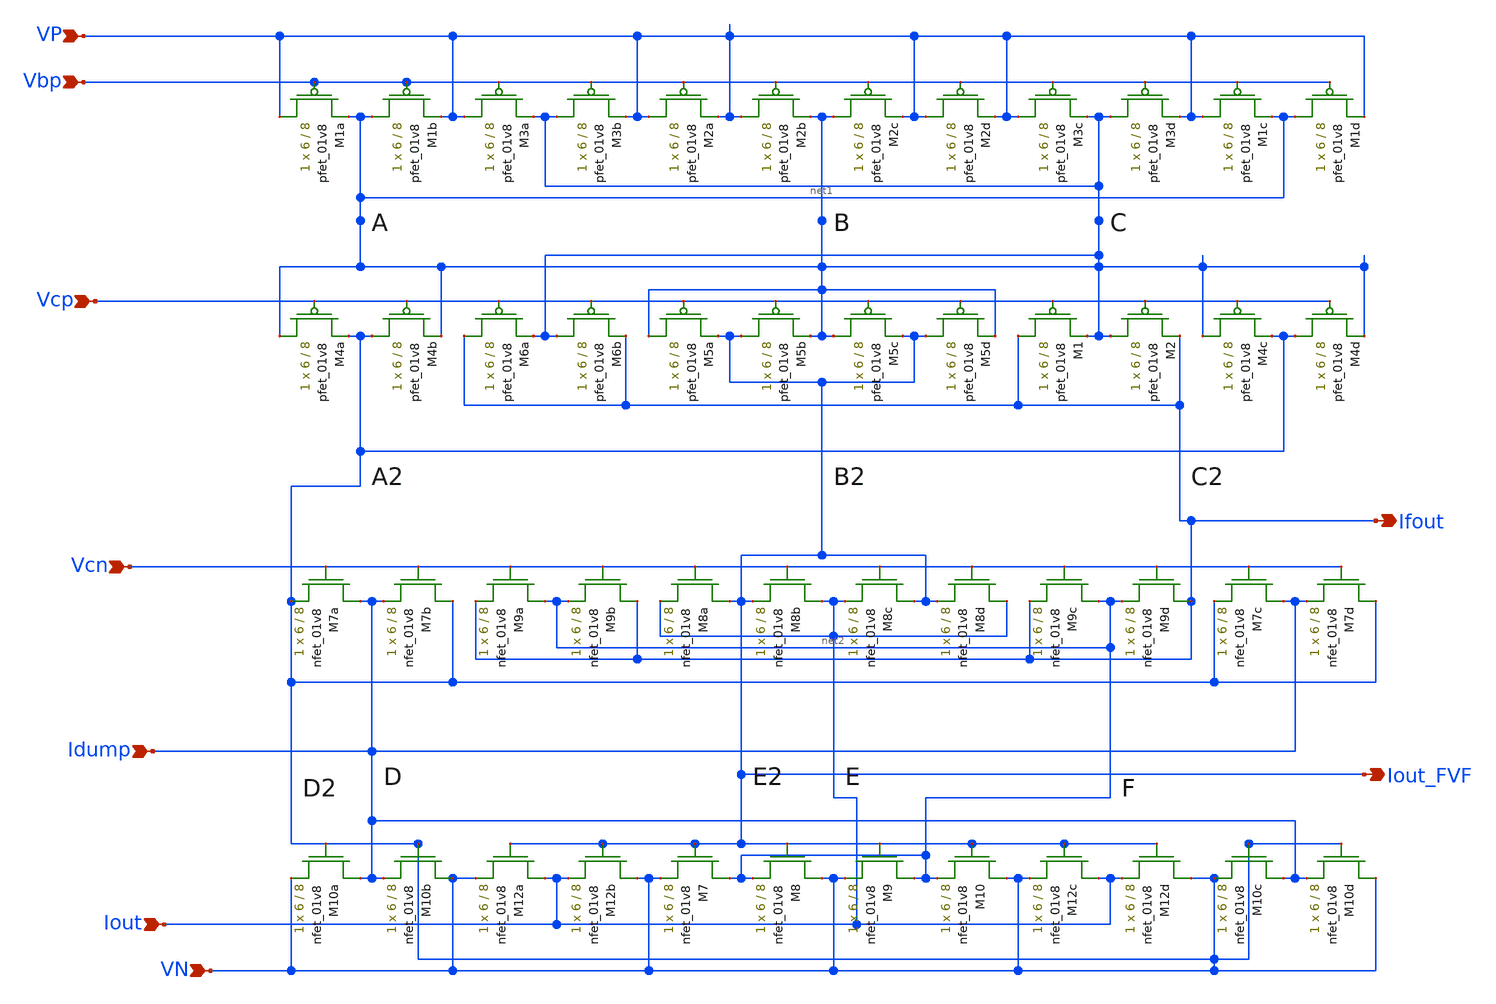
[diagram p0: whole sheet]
** sch_path: xschem/lds/lds-fvf-j.sch
**.subckt lds-fvf-j Vbp VP Vcp Vcn VN Idump Iout Ifout Iout_FVF
*.ipin Vbp
*.ipin VP
*.ipin Vcp
*.ipin Vcn
*.ipin VN
*.ipin Idump
*.ipin Iout
*.opin Ifout
*.opin Iout_FVF
XM1a VP Vbp net1 VDD sky130_fd_pr__pfet_01v8 L=8 W=6 nf=1 ad='int((nf+1)/2) * W/nf * 0.29' as='int((nf+2)/2) * W/nf * 0.29'
+ pd='2*int((nf+1)/2) * (W/nf + 0.29)' ps='2*int((nf+2)/2) * (W/nf + 0.29)' nrd='0.29 / W' nrs='0.29 / W'
+ sa=0 sb=0 sd=0 mult=1 m=1
XM1b net1 Vbp VP VDD sky130_fd_pr__pfet_01v8 L=8 W=6 nf=1 ad='int((nf+1)/2) * W/nf * 0.29' as='int((nf+2)/2) * W/nf * 0.29'
+ pd='2*int((nf+1)/2) * (W/nf + 0.29)' ps='2*int((nf+2)/2) * (W/nf + 0.29)' nrd='0.29 / W' nrs='0.29 / W'
+ sa=0 sb=0 sd=0 mult=1 m=1
XM3a VP Vbp net1 VDD sky130_fd_pr__pfet_01v8 L=8 W=6 nf=1 ad='int((nf+1)/2) * W/nf * 0.29' as='int((nf+2)/2) * W/nf * 0.29'
+ pd='2*int((nf+1)/2) * (W/nf + 0.29)' ps='2*int((nf+2)/2) * (W/nf + 0.29)' nrd='0.29 / W' nrs='0.29 / W'
+ sa=0 sb=0 sd=0 mult=1 m=1
XM3b net1 Vbp VP VDD sky130_fd_pr__pfet_01v8 L=8 W=6 nf=1 ad='int((nf+1)/2) * W/nf * 0.29' as='int((nf+2)/2) * W/nf * 0.29'
+ pd='2*int((nf+1)/2) * (W/nf + 0.29)' ps='2*int((nf+2)/2) * (W/nf + 0.29)' nrd='0.29 / W' nrs='0.29 / W'
+ sa=0 sb=0 sd=0 mult=1 m=1
XM2a VP Vbp VP VDD sky130_fd_pr__pfet_01v8 L=8 W=6 nf=1 ad='int((nf+1)/2) * W/nf * 0.29' as='int((nf+2)/2) * W/nf * 0.29'
+ pd='2*int((nf+1)/2) * (W/nf + 0.29)' ps='2*int((nf+2)/2) * (W/nf + 0.29)' nrd='0.29 / W' nrs='0.29 / W'
+ sa=0 sb=0 sd=0 mult=1 m=1
XM2b VP Vbp net1 VDD sky130_fd_pr__pfet_01v8 L=8 W=6 nf=1 ad='int((nf+1)/2) * W/nf * 0.29' as='int((nf+2)/2) * W/nf * 0.29'
+ pd='2*int((nf+1)/2) * (W/nf + 0.29)' ps='2*int((nf+2)/2) * (W/nf + 0.29)' nrd='0.29 / W' nrs='0.29 / W'
+ sa=0 sb=0 sd=0 mult=1 m=1
XM2c net1 Vbp VP VDD sky130_fd_pr__pfet_01v8 L=8 W=6 nf=1 ad='int((nf+1)/2) * W/nf * 0.29' as='int((nf+2)/2) * W/nf * 0.29'
+ pd='2*int((nf+1)/2) * (W/nf + 0.29)' ps='2*int((nf+2)/2) * (W/nf + 0.29)' nrd='0.29 / W' nrs='0.29 / W'
+ sa=0 sb=0 sd=0 mult=1 m=1
XM2d VP Vbp VP VDD sky130_fd_pr__pfet_01v8 L=8 W=6 nf=1 ad='int((nf+1)/2) * W/nf * 0.29' as='int((nf+2)/2) * W/nf * 0.29'
+ pd='2*int((nf+1)/2) * (W/nf + 0.29)' ps='2*int((nf+2)/2) * (W/nf + 0.29)' nrd='0.29 / W' nrs='0.29 / W'
+ sa=0 sb=0 sd=0 mult=1 m=1
XM3c VP Vbp net1 VDD sky130_fd_pr__pfet_01v8 L=8 W=6 nf=1 ad='int((nf+1)/2) * W/nf * 0.29' as='int((nf+2)/2) * W/nf * 0.29'
+ pd='2*int((nf+1)/2) * (W/nf + 0.29)' ps='2*int((nf+2)/2) * (W/nf + 0.29)' nrd='0.29 / W' nrs='0.29 / W'
+ sa=0 sb=0 sd=0 mult=1 m=1
XM3d net1 Vbp VP VDD sky130_fd_pr__pfet_01v8 L=8 W=6 nf=1 ad='int((nf+1)/2) * W/nf * 0.29' as='int((nf+2)/2) * W/nf * 0.29'
+ pd='2*int((nf+1)/2) * (W/nf + 0.29)' ps='2*int((nf+2)/2) * (W/nf + 0.29)' nrd='0.29 / W' nrs='0.29 / W'
+ sa=0 sb=0 sd=0 mult=1 m=1
XM1c VP Vbp net1 VDD sky130_fd_pr__pfet_01v8 L=8 W=6 nf=1 ad='int((nf+1)/2) * W/nf * 0.29' as='int((nf+2)/2) * W/nf * 0.29'
+ pd='2*int((nf+1)/2) * (W/nf + 0.29)' ps='2*int((nf+2)/2) * (W/nf + 0.29)' nrd='0.29 / W' nrs='0.29 / W'
+ sa=0 sb=0 sd=0 mult=1 m=1
XM1d net1 Vbp VP VDD sky130_fd_pr__pfet_01v8 L=8 W=6 nf=1 ad='int((nf+1)/2) * W/nf * 0.29' as='int((nf+2)/2) * W/nf * 0.29'
+ pd='2*int((nf+1)/2) * (W/nf + 0.29)' ps='2*int((nf+2)/2) * (W/nf + 0.29)' nrd='0.29 / W' nrs='0.29 / W'
+ sa=0 sb=0 sd=0 mult=1 m=1
XM4a net1 Vcp VN VDD sky130_fd_pr__pfet_01v8 L=8 W=6 nf=1 ad='int((nf+1)/2) * W/nf * 0.29' as='int((nf+2)/2) * W/nf * 0.29'
+ pd='2*int((nf+1)/2) * (W/nf + 0.29)' ps='2*int((nf+2)/2) * (W/nf + 0.29)' nrd='0.29 / W' nrs='0.29 / W'
+ sa=0 sb=0 sd=0 mult=1 m=1
XM4b VN Vcp net1 VDD sky130_fd_pr__pfet_01v8 L=8 W=6 nf=1 ad='int((nf+1)/2) * W/nf * 0.29' as='int((nf+2)/2) * W/nf * 0.29'
+ pd='2*int((nf+1)/2) * (W/nf + 0.29)' ps='2*int((nf+2)/2) * (W/nf + 0.29)' nrd='0.29 / W' nrs='0.29 / W'
+ sa=0 sb=0 sd=0 mult=1 m=1
XM6a Ifout Vcp net1 VDD sky130_fd_pr__pfet_01v8 L=8 W=6 nf=1 ad='int((nf+1)/2) * W/nf * 0.29' as='int((nf+2)/2) * W/nf * 0.29'
+ pd='2*int((nf+1)/2) * (W/nf + 0.29)' ps='2*int((nf+2)/2) * (W/nf + 0.29)' nrd='0.29 / W' nrs='0.29 / W'
+ sa=0 sb=0 sd=0 mult=1 m=1
XM6b net1 Vcp Ifout VDD sky130_fd_pr__pfet_01v8 L=8 W=6 nf=1 ad='int((nf+1)/2) * W/nf * 0.29' as='int((nf+2)/2) * W/nf * 0.29'
+ pd='2*int((nf+1)/2) * (W/nf + 0.29)' ps='2*int((nf+2)/2) * (W/nf + 0.29)' nrd='0.29 / W' nrs='0.29 / W'
+ sa=0 sb=0 sd=0 mult=1 m=1
XM5a net1 Vcp Iout_FVF VDD sky130_fd_pr__pfet_01v8 L=8 W=6 nf=1 ad='int((nf+1)/2) * W/nf * 0.29' as='int((nf+2)/2) * W/nf * 0.29'
+ pd='2*int((nf+1)/2) * (W/nf + 0.29)' ps='2*int((nf+2)/2) * (W/nf + 0.29)' nrd='0.29 / W' nrs='0.29 / W'
+ sa=0 sb=0 sd=0 mult=1 m=1
XM5b Iout_FVF Vcp net1 VDD sky130_fd_pr__pfet_01v8 L=8 W=6 nf=1 ad='int((nf+1)/2) * W/nf * 0.29' as='int((nf+2)/2) * W/nf * 0.29'
+ pd='2*int((nf+1)/2) * (W/nf + 0.29)' ps='2*int((nf+2)/2) * (W/nf + 0.29)' nrd='0.29 / W' nrs='0.29 / W'
+ sa=0 sb=0 sd=0 mult=1 m=1
XM5c net1 Vcp Iout_FVF VDD sky130_fd_pr__pfet_01v8 L=8 W=6 nf=1 ad='int((nf+1)/2) * W/nf * 0.29' as='int((nf+2)/2) * W/nf * 0.29'
+ pd='2*int((nf+1)/2) * (W/nf + 0.29)' ps='2*int((nf+2)/2) * (W/nf + 0.29)' nrd='0.29 / W' nrs='0.29 / W'
+ sa=0 sb=0 sd=0 mult=1 m=1
XM5d Iout_FVF Vcp net1 VDD sky130_fd_pr__pfet_01v8 L=8 W=6 nf=1 ad='int((nf+1)/2) * W/nf * 0.29' as='int((nf+2)/2) * W/nf * 0.29'
+ pd='2*int((nf+1)/2) * (W/nf + 0.29)' ps='2*int((nf+2)/2) * (W/nf + 0.29)' nrd='0.29 / W' nrs='0.29 / W'
+ sa=0 sb=0 sd=0 mult=1 m=1
XM1 Ifout Vcp net1 VDD sky130_fd_pr__pfet_01v8 L=8 W=6 nf=1 ad='int((nf+1)/2) * W/nf * 0.29' as='int((nf+2)/2) * W/nf * 0.29'
+ pd='2*int((nf+1)/2) * (W/nf + 0.29)' ps='2*int((nf+2)/2) * (W/nf + 0.29)' nrd='0.29 / W' nrs='0.29 / W'
+ sa=0 sb=0 sd=0 mult=1 m=1
XM2 net1 Vcp Ifout VDD sky130_fd_pr__pfet_01v8 L=8 W=6 nf=1 ad='int((nf+1)/2) * W/nf * 0.29' as='int((nf+2)/2) * W/nf * 0.29'
+ pd='2*int((nf+1)/2) * (W/nf + 0.29)' ps='2*int((nf+2)/2) * (W/nf + 0.29)' nrd='0.29 / W' nrs='0.29 / W'
+ sa=0 sb=0 sd=0 mult=1 m=1
XM4c net1 Vcp VN VDD sky130_fd_pr__pfet_01v8 L=8 W=6 nf=1 ad='int((nf+1)/2) * W/nf * 0.29' as='int((nf+2)/2) * W/nf * 0.29'
+ pd='2*int((nf+1)/2) * (W/nf + 0.29)' ps='2*int((nf+2)/2) * (W/nf + 0.29)' nrd='0.29 / W' nrs='0.29 / W'
+ sa=0 sb=0 sd=0 mult=1 m=1
XM4d VN Vcp net1 VDD sky130_fd_pr__pfet_01v8 L=8 W=6 nf=1 ad='int((nf+1)/2) * W/nf * 0.29' as='int((nf+2)/2) * W/nf * 0.29'
+ pd='2*int((nf+1)/2) * (W/nf + 0.29)' ps='2*int((nf+2)/2) * (W/nf + 0.29)' nrd='0.29 / W' nrs='0.29 / W'
+ sa=0 sb=0 sd=0 mult=1 m=1
XM7a Idump Vcn VN GND sky130_fd_pr__nfet_01v8 L=8 W=6 nf=1 ad='int((nf+1)/2) * W/nf * 0.29' as='int((nf+2)/2) * W/nf * 0.29'
+ pd='2*int((nf+1)/2) * (W/nf + 0.29)' ps='2*int((nf+2)/2) * (W/nf + 0.29)' nrd='0.29 / W' nrs='0.29 / W'
+ sa=0 sb=0 sd=0 mult=1 m=1
XM7b VN Vcn Idump GND sky130_fd_pr__nfet_01v8 L=8 W=6 nf=1 ad='int((nf+1)/2) * W/nf * 0.29' as='int((nf+2)/2) * W/nf * 0.29'
+ pd='2*int((nf+1)/2) * (W/nf + 0.29)' ps='2*int((nf+2)/2) * (W/nf + 0.29)' nrd='0.29 / W' nrs='0.29 / W'
+ sa=0 sb=0 sd=0 mult=1 m=1
XM9a net2 Vcn Ifout GND sky130_fd_pr__nfet_01v8 L=8 W=6 nf=1 ad='int((nf+1)/2) * W/nf * 0.29' as='int((nf+2)/2) * W/nf * 0.29'
+ pd='2*int((nf+1)/2) * (W/nf + 0.29)' ps='2*int((nf+2)/2) * (W/nf + 0.29)' nrd='0.29 / W' nrs='0.29 / W'
+ sa=0 sb=0 sd=0 mult=1 m=1
XM9b Ifout Vcn net2 GND sky130_fd_pr__nfet_01v8 L=8 W=6 nf=1 ad='int((nf+1)/2) * W/nf * 0.29' as='int((nf+2)/2) * W/nf * 0.29'
+ pd='2*int((nf+1)/2) * (W/nf + 0.29)' ps='2*int((nf+2)/2) * (W/nf + 0.29)' nrd='0.29 / W' nrs='0.29 / W'
+ sa=0 sb=0 sd=0 mult=1 m=1
XM8a Iout_FVF Vcn Iout GND sky130_fd_pr__nfet_01v8 L=8 W=6 nf=1 ad='int((nf+1)/2) * W/nf * 0.29' as='int((nf+2)/2) * W/nf * 0.29'
+ pd='2*int((nf+1)/2) * (W/nf + 0.29)' ps='2*int((nf+2)/2) * (W/nf + 0.29)' nrd='0.29 / W' nrs='0.29 / W'
+ sa=0 sb=0 sd=0 mult=1 m=1
XM8b Iout Vcn Iout_FVF GND sky130_fd_pr__nfet_01v8 L=8 W=6 nf=1 ad='int((nf+1)/2) * W/nf * 0.29' as='int((nf+2)/2) * W/nf * 0.29'
+ pd='2*int((nf+1)/2) * (W/nf + 0.29)' ps='2*int((nf+2)/2) * (W/nf + 0.29)' nrd='0.29 / W' nrs='0.29 / W'
+ sa=0 sb=0 sd=0 mult=1 m=1
XM8c Iout_FVF Vcn Iout GND sky130_fd_pr__nfet_01v8 L=8 W=6 nf=1 ad='int((nf+1)/2) * W/nf * 0.29' as='int((nf+2)/2) * W/nf * 0.29'
+ pd='2*int((nf+1)/2) * (W/nf + 0.29)' ps='2*int((nf+2)/2) * (W/nf + 0.29)' nrd='0.29 / W' nrs='0.29 / W'
+ sa=0 sb=0 sd=0 mult=1 m=1
XM8d Iout Vcn Iout_FVF GND sky130_fd_pr__nfet_01v8 L=8 W=6 nf=1 ad='int((nf+1)/2) * W/nf * 0.29' as='int((nf+2)/2) * W/nf * 0.29'
+ pd='2*int((nf+1)/2) * (W/nf + 0.29)' ps='2*int((nf+2)/2) * (W/nf + 0.29)' nrd='0.29 / W' nrs='0.29 / W'
+ sa=0 sb=0 sd=0 mult=1 m=1
XM9c net2 Vcn Ifout GND sky130_fd_pr__nfet_01v8 L=8 W=6 nf=1 ad='int((nf+1)/2) * W/nf * 0.29' as='int((nf+2)/2) * W/nf * 0.29'
+ pd='2*int((nf+1)/2) * (W/nf + 0.29)' ps='2*int((nf+2)/2) * (W/nf + 0.29)' nrd='0.29 / W' nrs='0.29 / W'
+ sa=0 sb=0 sd=0 mult=1 m=1
XM9d Ifout Vcn net2 GND sky130_fd_pr__nfet_01v8 L=8 W=6 nf=1 ad='int((nf+1)/2) * W/nf * 0.29' as='int((nf+2)/2) * W/nf * 0.29'
+ pd='2*int((nf+1)/2) * (W/nf + 0.29)' ps='2*int((nf+2)/2) * (W/nf + 0.29)' nrd='0.29 / W' nrs='0.29 / W'
+ sa=0 sb=0 sd=0 mult=1 m=1
XM7c Idump Vcn VN GND sky130_fd_pr__nfet_01v8 L=8 W=6 nf=1 ad='int((nf+1)/2) * W/nf * 0.29' as='int((nf+2)/2) * W/nf * 0.29'
+ pd='2*int((nf+1)/2) * (W/nf + 0.29)' ps='2*int((nf+2)/2) * (W/nf + 0.29)' nrd='0.29 / W' nrs='0.29 / W'
+ sa=0 sb=0 sd=0 mult=1 m=1
XM7d VN Vcn Idump GND sky130_fd_pr__nfet_01v8 L=8 W=6 nf=1 ad='int((nf+1)/2) * W/nf * 0.29' as='int((nf+2)/2) * W/nf * 0.29'
+ pd='2*int((nf+1)/2) * (W/nf + 0.29)' ps='2*int((nf+2)/2) * (W/nf + 0.29)' nrd='0.29 / W' nrs='0.29 / W'
+ sa=0 sb=0 sd=0 mult=1 m=1
XM10a Idump VN VN GND sky130_fd_pr__nfet_01v8 L=8 W=6 nf=1 ad='int((nf+1)/2) * W/nf * 0.29' as='int((nf+2)/2) * W/nf * 0.29'
+ pd='2*int((nf+1)/2) * (W/nf + 0.29)' ps='2*int((nf+2)/2) * (W/nf + 0.29)' nrd='0.29 / W' nrs='0.29 / W'
+ sa=0 sb=0 sd=0 mult=1 m=1
XM10b VN VN Idump GND sky130_fd_pr__nfet_01v8 L=8 W=6 nf=1 ad='int((nf+1)/2) * W/nf * 0.29' as='int((nf+2)/2) * W/nf * 0.29'
+ pd='2*int((nf+1)/2) * (W/nf + 0.29)' ps='2*int((nf+2)/2) * (W/nf + 0.29)' nrd='0.29 / W' nrs='0.29 / W'
+ sa=0 sb=0 sd=0 mult=1 m=1
XM12a Iout Iout_FVF VN GND sky130_fd_pr__nfet_01v8 L=8 W=6 nf=1 ad='int((nf+1)/2) * W/nf * 0.29' as='int((nf+2)/2) * W/nf * 0.29'
+ pd='2*int((nf+1)/2) * (W/nf + 0.29)' ps='2*int((nf+2)/2) * (W/nf + 0.29)' nrd='0.29 / W' nrs='0.29 / W'
+ sa=0 sb=0 sd=0 mult=1 m=1
XM12b VN Iout_FVF Iout GND sky130_fd_pr__nfet_01v8 L=8 W=6 nf=1 ad='int((nf+1)/2) * W/nf * 0.29' as='int((nf+2)/2) * W/nf * 0.29'
+ pd='2*int((nf+1)/2) * (W/nf + 0.29)' ps='2*int((nf+2)/2) * (W/nf + 0.29)' nrd='0.29 / W' nrs='0.29 / W'
+ sa=0 sb=0 sd=0 mult=1 m=1
XM7 net2 Iout_FVF VN GND sky130_fd_pr__nfet_01v8 L=8 W=6 nf=1 ad='int((nf+1)/2) * W/nf * 0.29' as='int((nf+2)/2) * W/nf * 0.29'
+ pd='2*int((nf+1)/2) * (W/nf + 0.29)' ps='2*int((nf+2)/2) * (W/nf + 0.29)' nrd='0.29 / W' nrs='0.29 / W'
+ sa=0 sb=0 sd=0 mult=1 m=1
XM8 VN Iout_FVF net2 GND sky130_fd_pr__nfet_01v8 L=8 W=6 nf=1 ad='int((nf+1)/2) * W/nf * 0.29' as='int((nf+2)/2) * W/nf * 0.29'
+ pd='2*int((nf+1)/2) * (W/nf + 0.29)' ps='2*int((nf+2)/2) * (W/nf + 0.29)' nrd='0.29 / W' nrs='0.29 / W'
+ sa=0 sb=0 sd=0 mult=1 m=1
XM9 net2 Iout_FVF VN GND sky130_fd_pr__nfet_01v8 L=8 W=6 nf=1 ad='int((nf+1)/2) * W/nf * 0.29' as='int((nf+2)/2) * W/nf * 0.29'
+ pd='2*int((nf+1)/2) * (W/nf + 0.29)' ps='2*int((nf+2)/2) * (W/nf + 0.29)' nrd='0.29 / W' nrs='0.29 / W'
+ sa=0 sb=0 sd=0 mult=1 m=1
XM10 VN Iout_FVF net2 GND sky130_fd_pr__nfet_01v8 L=8 W=6 nf=1 ad='int((nf+1)/2) * W/nf * 0.29' as='int((nf+2)/2) * W/nf * 0.29'
+ pd='2*int((nf+1)/2) * (W/nf + 0.29)' ps='2*int((nf+2)/2) * (W/nf + 0.29)' nrd='0.29 / W' nrs='0.29 / W'
+ sa=0 sb=0 sd=0 mult=1 m=1
XM12c Iout Iout_FVF VN GND sky130_fd_pr__nfet_01v8 L=8 W=6 nf=1 ad='int((nf+1)/2) * W/nf * 0.29' as='int((nf+2)/2) * W/nf * 0.29'
+ pd='2*int((nf+1)/2) * (W/nf + 0.29)' ps='2*int((nf+2)/2) * (W/nf + 0.29)' nrd='0.29 / W' nrs='0.29 / W'
+ sa=0 sb=0 sd=0 mult=1 m=1
XM12d VN Iout_FVF Iout GND sky130_fd_pr__nfet_01v8 L=8 W=6 nf=1 ad='int((nf+1)/2) * W/nf * 0.29' as='int((nf+2)/2) * W/nf * 0.29'
+ pd='2*int((nf+1)/2) * (W/nf + 0.29)' ps='2*int((nf+2)/2) * (W/nf + 0.29)' nrd='0.29 / W' nrs='0.29 / W'
+ sa=0 sb=0 sd=0 mult=1 m=1
XM10c Idump VN VN GND sky130_fd_pr__nfet_01v8 L=8 W=6 nf=1 ad='int((nf+1)/2) * W/nf * 0.29' as='int((nf+2)/2) * W/nf * 0.29'
+ pd='2*int((nf+1)/2) * (W/nf + 0.29)' ps='2*int((nf+2)/2) * (W/nf + 0.29)' nrd='0.29 / W' nrs='0.29 / W'
+ sa=0 sb=0 sd=0 mult=1 m=1
XM10d VN VN Idump GND sky130_fd_pr__nfet_01v8 L=8 W=6 nf=1 ad='int((nf+1)/2) * W/nf * 0.29' as='int((nf+2)/2) * W/nf * 0.29'
+ pd='2*int((nf+1)/2) * (W/nf + 0.29)' ps='2*int((nf+2)/2) * (W/nf + 0.29)' nrd='0.29 / W' nrs='0.29 / W'
+ sa=0 sb=0 sd=0 mult=1 m=1
**.ends
.end
